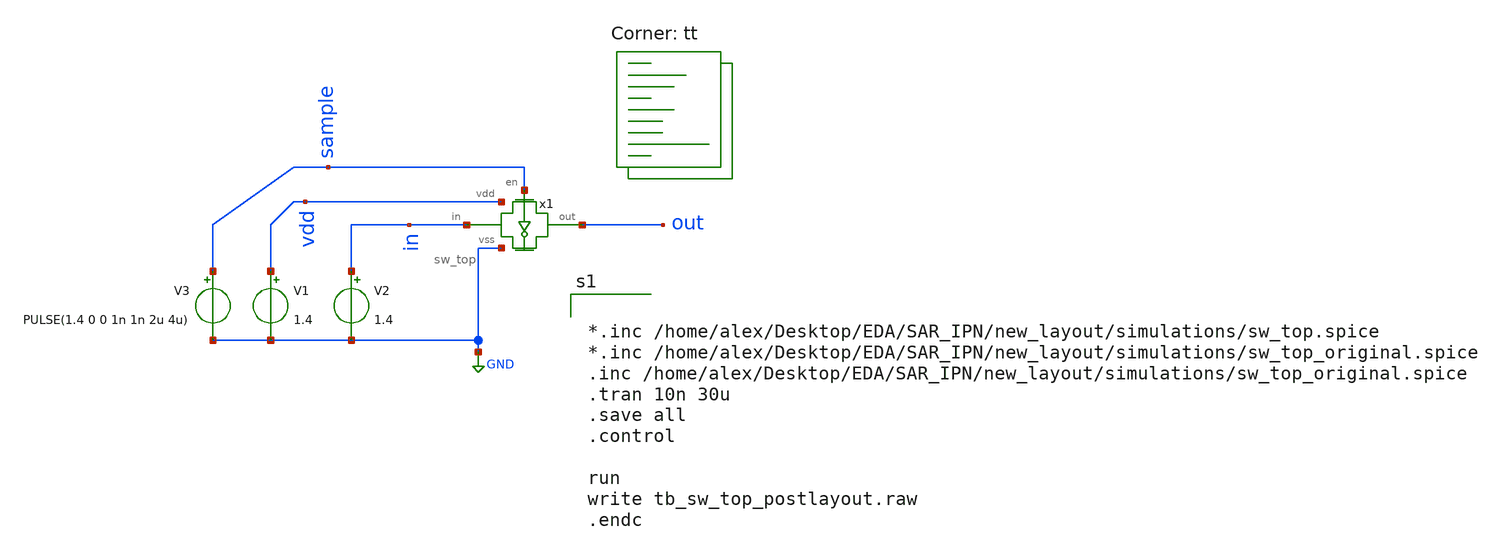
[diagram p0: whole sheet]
** sch_path: new_layout/simulations/tb_sw_top_postlayout.sch
**.subckt tb_sw_top_postlayout
x1 out sample GND in vdd sw_top
V1 vdd GND 1.4
V2 in GND 1.4
V3 sample GND PULSE(1.4 0 0 1n 1n 2u 4u)
**** begin user architecture code


*.inc /home/alex/Desktop/EDA/SAR_IPN/new_layout/simulations/sw_top.spice
*.inc /home/alex/Desktop/EDA/SAR_IPN/new_layout/simulations/sw_top_original.spice
.inc /home/alex/Desktop/EDA/SAR_IPN/new_layout/simulations/sw_top_original.spice
.tran 10n 30u
.save all
.control

run
write tb_sw_top_postlayout.raw
.endc


.lib $::SKYWATER_MODELS/sky130.lib.spice tt
**** end user architecture code
**.ends
.GLOBAL GND
.end
